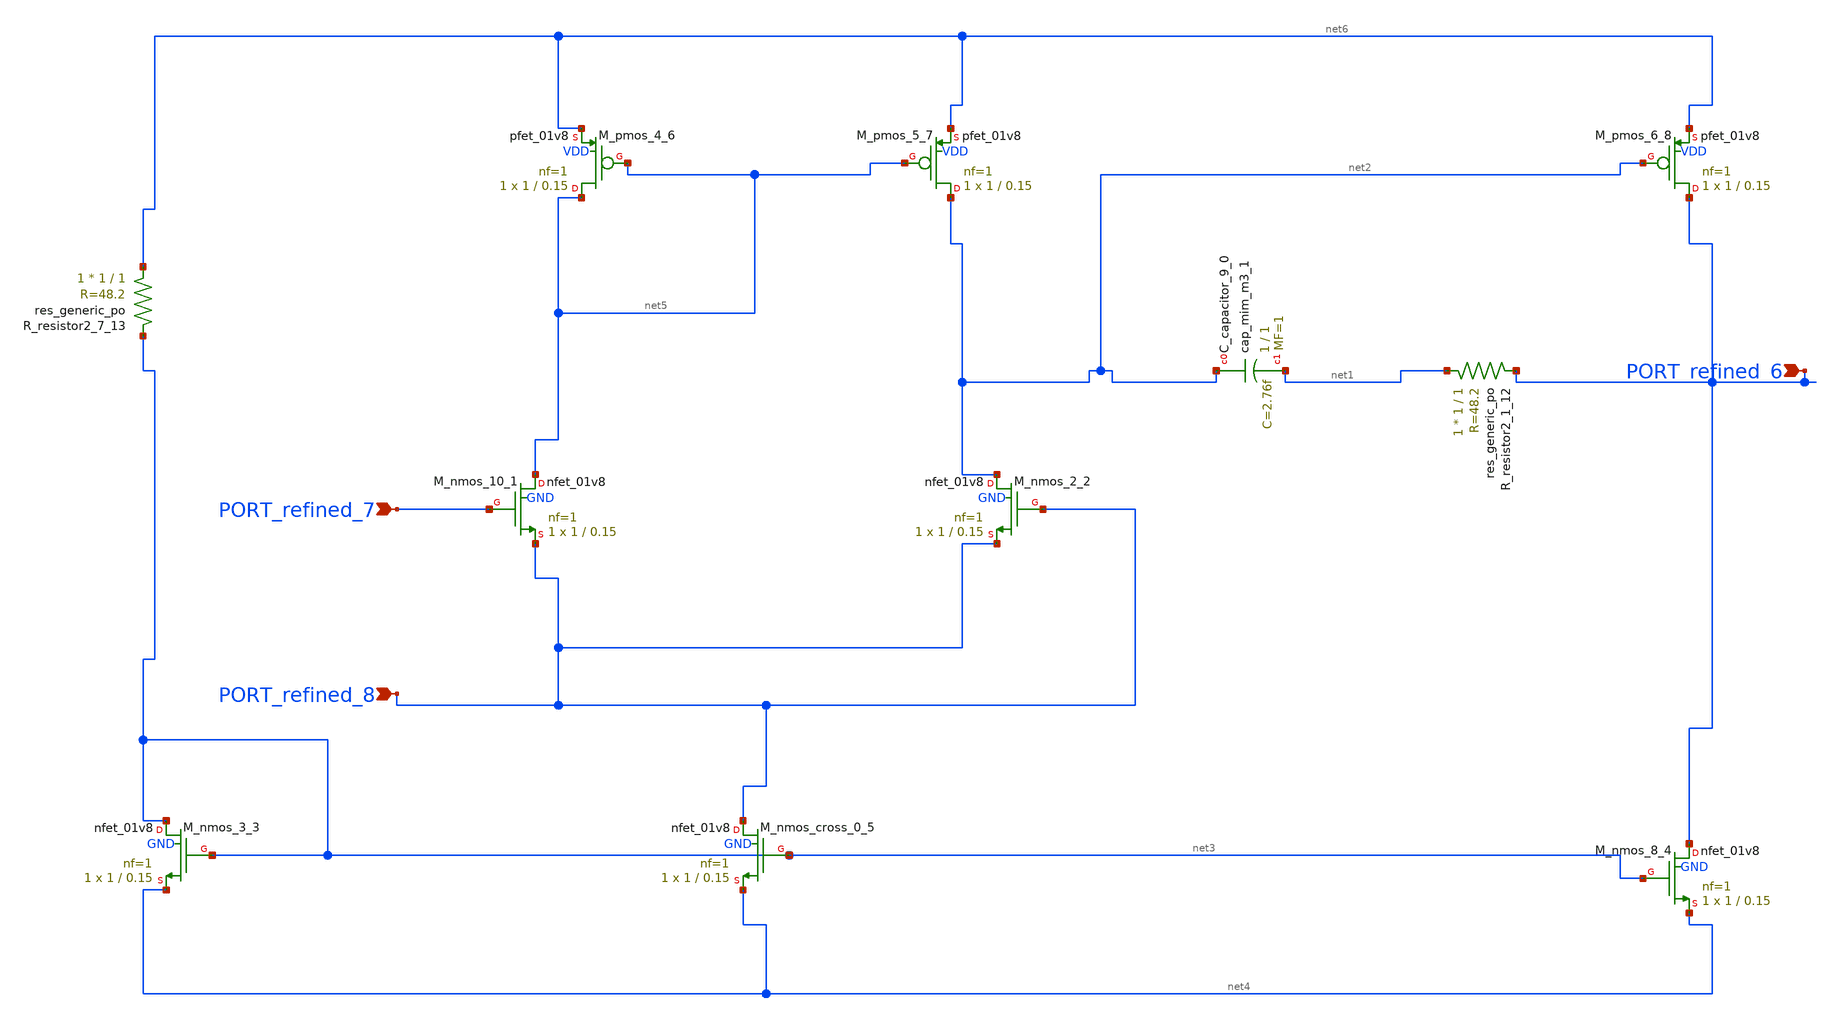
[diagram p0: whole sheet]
** sch_path: schematics/Image2Net/032.sch
**.subckt 032 PORT_refined_7 PORT_refined_8 PORT_refined_6
*.ipin PORT_refined_7
*.ipin PORT_refined_8
*.ipin PORT_refined_6
XC_capacitor_9_0 net2 net1 sky130_fd_pr__cap_mim_m3_1 W=1 L=1 MF=1 m=1
XM_nmos_10_1 net5 PORT_refined_7 PORT_refined_8 GND sky130_fd_pr__nfet_01v8 L=0.15 W=1 nf=1 ad='int((1 + 1)/2) * 1 / 1 * 0.29'
+ as='int((1 + 2)/2) * 1 / 1 * 0.29' pd='2*int((1 + 1)/2) * (1 / 1 + 0.29)' ps='2*int((1 + 2)/2) * (1 / 1 + 0.29)'
+ nrd='0.29 / 1 ' nrs='0.29 / 1 ' sa=0 sb=0 sd=0 mult=1 m=1
XM_nmos_2_2 net2 PORT_refined_8 PORT_refined_8 GND sky130_fd_pr__nfet_01v8 L=0.15 W=1 nf=1 ad='int((1 + 1)/2) * 1 / 1 * 0.29'
+ as='int((1 + 2)/2) * 1 / 1 * 0.29' pd='2*int((1 + 1)/2) * (1 / 1 + 0.29)' ps='2*int((1 + 2)/2) * (1 / 1 + 0.29)'
+ nrd='0.29 / 1 ' nrs='0.29 / 1 ' sa=0 sb=0 sd=0 mult=1 m=1
XM_nmos_3_3 net3 net3 net4 GND sky130_fd_pr__nfet_01v8 L=0.15 W=1 nf=1 ad='int((1 + 1)/2) * 1 / 1 * 0.29'
+ as='int((1 + 2)/2) * 1 / 1 * 0.29' pd='2*int((1 + 1)/2) * (1 / 1 + 0.29)' ps='2*int((1 + 2)/2) * (1 / 1 + 0.29)'
+ nrd='0.29 / 1 ' nrs='0.29 / 1 ' sa=0 sb=0 sd=0 mult=1 m=1
XM_nmos_8_4 PORT_refined_6 net3 net4 GND sky130_fd_pr__nfet_01v8 L=0.15 W=1 nf=1 ad='int((1 + 1)/2) * 1 / 1 * 0.29'
+ as='int((1 + 2)/2) * 1 / 1 * 0.29' pd='2*int((1 + 1)/2) * (1 / 1 + 0.29)' ps='2*int((1 + 2)/2) * (1 / 1 + 0.29)'
+ nrd='0.29 / 1 ' nrs='0.29 / 1 ' sa=0 sb=0 sd=0 mult=1 m=1
XM_nmos_cross_0_5 PORT_refined_8 net3 net4 GND sky130_fd_pr__nfet_01v8 L=0.15 W=1 nf=1 ad='int((1 + 1)/2) * 1 / 1 * 0.29'
+ as='int((1 + 2)/2) * 1 / 1 * 0.29' pd='2*int((1 + 1)/2) * (1 / 1 + 0.29)' ps='2*int((1 + 2)/2) * (1 / 1 + 0.29)'
+ nrd='0.29 / 1 ' nrs='0.29 / 1 ' sa=0 sb=0 sd=0 mult=1 m=1
XM_pmos_4_6 net5 net5 net6 VDD sky130_fd_pr__pfet_01v8 L=0.15 W=1 nf=1 ad='int((1 + 1)/2) * 1 / 1 * 0.29'
+ as='int((1 + 2)/2) * 1 / 1 * 0.29' pd='2*int((1 + 1)/2) * (1 / 1 + 0.29)' ps='2*int((1 + 2)/2) * (1 / 1 + 0.29)'
+ nrd='0.29 / 1 ' nrs='0.29 / 1 ' sa=0 sb=0 sd=0 mult=1 m=1
XM_pmos_5_7 net2 net5 net6 VDD sky130_fd_pr__pfet_01v8 L=0.15 W=1 nf=1 ad='int((1 + 1)/2) * 1 / 1 * 0.29'
+ as='int((1 + 2)/2) * 1 / 1 * 0.29' pd='2*int((1 + 1)/2) * (1 / 1 + 0.29)' ps='2*int((1 + 2)/2) * (1 / 1 + 0.29)'
+ nrd='0.29 / 1 ' nrs='0.29 / 1 ' sa=0 sb=0 sd=0 mult=1 m=1
XM_pmos_6_8 PORT_refined_6 net2 net6 VDD sky130_fd_pr__pfet_01v8 L=0.15 W=1 nf=1 ad='int((1 + 1)/2) * 1 / 1 * 0.29'
+ as='int((1 + 2)/2) * 1 / 1 * 0.29' pd='2*int((1 + 1)/2) * (1 / 1 + 0.29)' ps='2*int((1 + 2)/2) * (1 / 1 + 0.29)'
+ nrd='0.29 / 1 ' nrs='0.29 / 1 ' sa=0 sb=0 sd=0 mult=1 m=1
XR_resistor2_1_12 net1 PORT_refined_6 sky130_fd_pr__res_generic_po W=1 L=1 m=1
XR_resistor2_7_13 net6 net3 sky130_fd_pr__res_generic_po W=1 L=1 m=1
**.ends
.end
